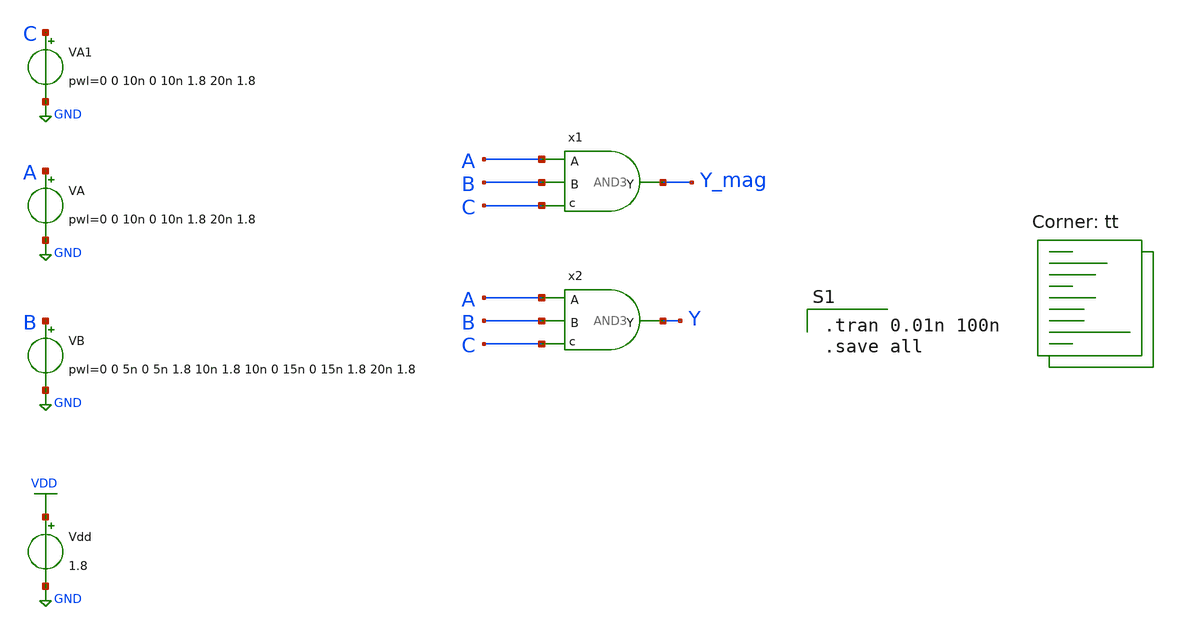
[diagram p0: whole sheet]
** sch_path: gates/and3magicsim.sch
**.subckt and3magicsim
Vdd VDD GND 1.8
VA A GND pwl=0 0 10n 0 10n 1.8 20n 1.8
VB B GND pwl=0 0 5n 0 5n 1.8 10n 1.8 10n 0 15n 0 15n 1.8 20n 1.8
x1 A Y_mag B C AND3
x2 A Y B C AND3_GATE_parax
VA1 C GND pwl=0 0 10n 0 10n 1.8 20n 1.8
**** begin user architecture code

.tran 0.01n 100n
.save all

.lib $::SKYWATER_MODELS/sky130.lib.spice tt
**** end user architecture code
**.ends

* expanding   symbol:  AND3.sym # of pins=4
** sym_path: gates/AND3.sym
** sch_path: gates/AND3.sch
.subckt AND3 A Y B c
*.ipin A
*.ipin B
*.opin Y
*.ipin c
XM1 net1 A net2 GND sky130_fd_pr__nfet_01v8 L=0.15 W=1 nf=1 ad='int((nf+1)/2) * W/nf * 0.29' as='int((nf+2)/2) * W/nf * 0.29'
+ pd='2*int((nf+1)/2) * (W/nf + 0.29)' ps='2*int((nf+2)/2) * (W/nf + 0.29)' nrd='0.29 / W' nrs='0.29 / W'
+ sa=0 sb=0 sd=0 mult=1 m=1
XM2 net2 B net3 GND sky130_fd_pr__nfet_01v8 L=0.15 W=1 nf=1 ad='int((nf+1)/2) * W/nf * 0.29' as='int((nf+2)/2) * W/nf * 0.29'
+ pd='2*int((nf+1)/2) * (W/nf + 0.29)' ps='2*int((nf+2)/2) * (W/nf + 0.29)' nrd='0.29 / W' nrs='0.29 / W'
+ sa=0 sb=0 sd=0 mult=1 m=1
XM3 net1 A VDD VDD sky130_fd_pr__pfet_01v8 L=0.15 W=1 nf=1 ad='int((nf+1)/2) * W/nf * 0.29' as='int((nf+2)/2) * W/nf * 0.29'
+ pd='2*int((nf+1)/2) * (W/nf + 0.29)' ps='2*int((nf+2)/2) * (W/nf + 0.29)' nrd='0.29 / W' nrs='0.29 / W'
+ sa=0 sb=0 sd=0 mult=1 m=1
XM4 net1 B VDD VDD sky130_fd_pr__pfet_01v8 L=0.15 W=1 nf=1 ad='int((nf+1)/2) * W/nf * 0.29' as='int((nf+2)/2) * W/nf * 0.29'
+ pd='2*int((nf+1)/2) * (W/nf + 0.29)' ps='2*int((nf+2)/2) * (W/nf + 0.29)' nrd='0.29 / W' nrs='0.29 / W'
+ sa=0 sb=0 sd=0 mult=1 m=1
XM5 net1 c VDD VDD sky130_fd_pr__pfet_01v8 L=0.15 W=1 nf=1 ad='int((nf+1)/2) * W/nf * 0.29' as='int((nf+2)/2) * W/nf * 0.29'
+ pd='2*int((nf+1)/2) * (W/nf + 0.29)' ps='2*int((nf+2)/2) * (W/nf + 0.29)' nrd='0.29 / W' nrs='0.29 / W'
+ sa=0 sb=0 sd=0 mult=1 m=1
XM6 net3 c GND GND sky130_fd_pr__nfet_01v8 L=0.15 W=1 nf=1 ad='int((nf+1)/2) * W/nf * 0.29' as='int((nf+2)/2) * W/nf * 0.29'
+ pd='2*int((nf+1)/2) * (W/nf + 0.29)' ps='2*int((nf+2)/2) * (W/nf + 0.29)' nrd='0.29 / W' nrs='0.29 / W'
+ sa=0 sb=0 sd=0 mult=1 m=1
X1 net1 Y inv_vtc
.ends


* expanding   symbol:  AND3_GATE_parax.sym # of pins=4
** sym_path: gates/AND3.sym
.include [file normalize /home/apn/mag_gates/AND3_GATE_parax.spice]

* expanding   symbol:  /home/apn/test_xschem_sky130/inv_vtc.sym # of pins=2
** sym_path: gates/inv_vtc.sym
** sch_path: gates/inv_vtc.sch
.subckt inv_vtc A Y
*.ipin A
*.opin Y
XM1 Y A VDD VDD sky130_fd_pr__pfet_01v8 L=0.15 W=2 nf=1 ad='int((nf+1)/2) * W/nf * 0.29' as='int((nf+2)/2) * W/nf * 0.29'
+ pd='2*int((nf+1)/2) * (W/nf + 0.29)' ps='2*int((nf+2)/2) * (W/nf + 0.29)' nrd='0.29 / W' nrs='0.29 / W'
+ sa=0 sb=0 sd=0 mult=1 m=1
XM2 Y A GND GND sky130_fd_pr__nfet_01v8 L=0.15 W=1 nf=1 ad='int((nf+1)/2) * W/nf * 0.29' as='int((nf+2)/2) * W/nf * 0.29'
+ pd='2*int((nf+1)/2) * (W/nf + 0.29)' ps='2*int((nf+2)/2) * (W/nf + 0.29)' nrd='0.29 / W' nrs='0.29 / W'
+ sa=0 sb=0 sd=0 mult=1 m=1
.ends

.GLOBAL VDD
.GLOBAL GND
.end
